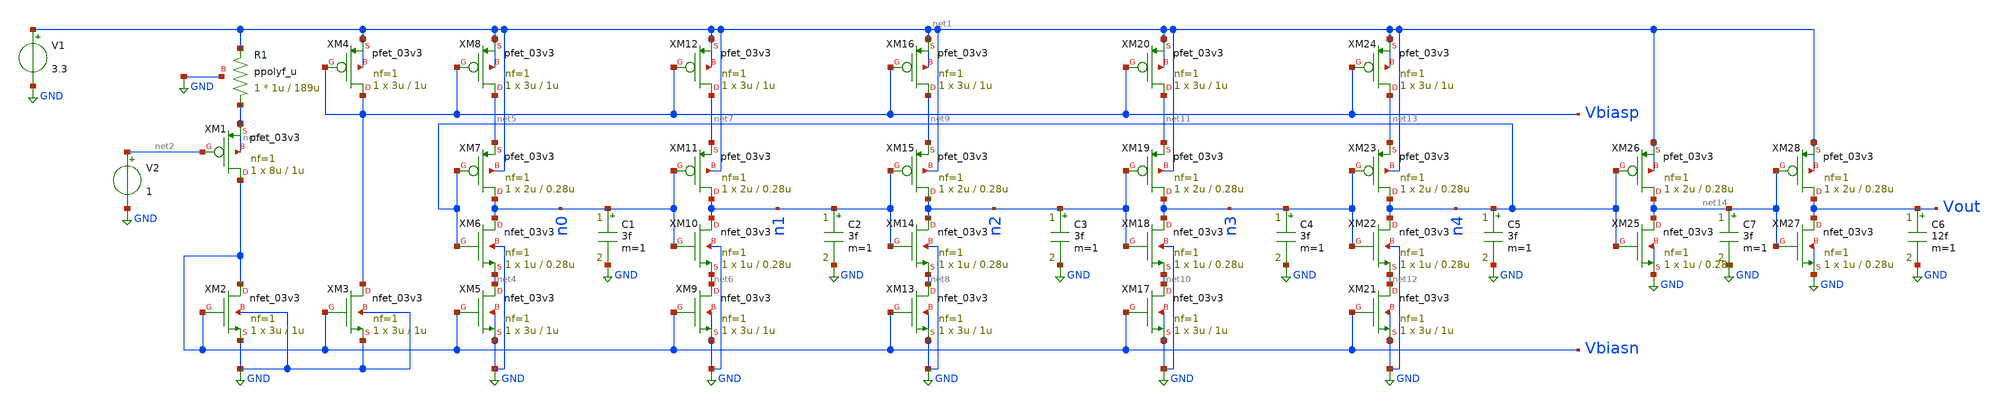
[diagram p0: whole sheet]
** sch_path: analog/vco/vco.sch
**.subckt vco
XM1 Vbiasn net2 net3 net3 pfet_03v3 L=1u W=8u nf=1 ad='int((nf+1)/2) * W/nf * 0.18u' as='int((nf+2)/2) * W/nf * 0.18u'
+ pd='2*int((nf+1)/2) * (W/nf + 0.18u)' ps='2*int((nf+2)/2) * (W/nf + 0.18u)' nrd='0.18u / W' nrs='0.18u / W'
+ sa=0 sb=0 sd=0 m=1
XM2 Vbiasn Vbiasn GND GND nfet_03v3 L=1u W=3u nf=1 ad='int((nf+1)/2) * W/nf * 0.18u' as='int((nf+2)/2) * W/nf * 0.18u'
+ pd='2*int((nf+1)/2) * (W/nf + 0.18u)' ps='2*int((nf+2)/2) * (W/nf + 0.18u)' nrd='0.18u / W' nrs='0.18u / W'
+ sa=0 sb=0 sd=0 m=1
XM3 Vbiasp Vbiasn GND GND nfet_03v3 L=1u W=3u nf=1 ad='int((nf+1)/2) * W/nf * 0.18u' as='int((nf+2)/2) * W/nf * 0.18u'
+ pd='2*int((nf+1)/2) * (W/nf + 0.18u)' ps='2*int((nf+2)/2) * (W/nf + 0.18u)' nrd='0.18u / W' nrs='0.18u / W'
+ sa=0 sb=0 sd=0 m=1
V1 net1 GND 3.3
XM4 Vbiasp Vbiasp net1 net1 pfet_03v3 L=1u W=3u nf=1 ad='int((nf+1)/2) * W/nf * 0.18u' as='int((nf+2)/2) * W/nf * 0.18u'
+ pd='2*int((nf+1)/2) * (W/nf + 0.18u)' ps='2*int((nf+2)/2) * (W/nf + 0.18u)' nrd='0.18u / W' nrs='0.18u / W'
+ sa=0 sb=0 sd=0 m=1
V2 net2 GND 1
XR1 net3 net1 GND ppolyf_u r_width=1u r_length=189u m=1
XM5 net4 Vbiasn GND GND nfet_03v3 L=1u W=3u nf=1 ad='int((nf+1)/2) * W/nf * 0.18u' as='int((nf+2)/2) * W/nf * 0.18u'
+ pd='2*int((nf+1)/2) * (W/nf + 0.18u)' ps='2*int((nf+2)/2) * (W/nf + 0.18u)' nrd='0.18u / W' nrs='0.18u / W'
+ sa=0 sb=0 sd=0 m=1
XM6 n0 n4 net4 GND nfet_03v3 L=0.28u W=1u nf=1 ad='int((nf+1)/2) * W/nf * 0.18u' as='int((nf+2)/2) * W/nf * 0.18u'
+ pd='2*int((nf+1)/2) * (W/nf + 0.18u)' ps='2*int((nf+2)/2) * (W/nf + 0.18u)' nrd='0.18u / W' nrs='0.18u / W'
+ sa=0 sb=0 sd=0 m=1
XM7 n0 n4 net5 net1 pfet_03v3 L=0.28u W=2u nf=1 ad='int((nf+1)/2) * W/nf * 0.18u' as='int((nf+2)/2) * W/nf * 0.18u'
+ pd='2*int((nf+1)/2) * (W/nf + 0.18u)' ps='2*int((nf+2)/2) * (W/nf + 0.18u)' nrd='0.18u / W' nrs='0.18u / W'
+ sa=0 sb=0 sd=0 m=1
XM8 net5 Vbiasp net1 net1 pfet_03v3 L=1u W=3u nf=1 ad='int((nf+1)/2) * W/nf * 0.18u' as='int((nf+2)/2) * W/nf * 0.18u'
+ pd='2*int((nf+1)/2) * (W/nf + 0.18u)' ps='2*int((nf+2)/2) * (W/nf + 0.18u)' nrd='0.18u / W' nrs='0.18u / W'
+ sa=0 sb=0 sd=0 m=1
XM9 net6 Vbiasn GND GND nfet_03v3 L=1u W=3u nf=1 ad='int((nf+1)/2) * W/nf * 0.18u' as='int((nf+2)/2) * W/nf * 0.18u'
+ pd='2*int((nf+1)/2) * (W/nf + 0.18u)' ps='2*int((nf+2)/2) * (W/nf + 0.18u)' nrd='0.18u / W' nrs='0.18u / W'
+ sa=0 sb=0 sd=0 m=1
XM10 n1 n0 net6 GND nfet_03v3 L=0.28u W=1u nf=1 ad='int((nf+1)/2) * W/nf * 0.18u' as='int((nf+2)/2) * W/nf * 0.18u'
+ pd='2*int((nf+1)/2) * (W/nf + 0.18u)' ps='2*int((nf+2)/2) * (W/nf + 0.18u)' nrd='0.18u / W' nrs='0.18u / W'
+ sa=0 sb=0 sd=0 m=1
XM11 n1 n0 net7 net1 pfet_03v3 L=0.28u W=2u nf=1 ad='int((nf+1)/2) * W/nf * 0.18u' as='int((nf+2)/2) * W/nf * 0.18u'
+ pd='2*int((nf+1)/2) * (W/nf + 0.18u)' ps='2*int((nf+2)/2) * (W/nf + 0.18u)' nrd='0.18u / W' nrs='0.18u / W'
+ sa=0 sb=0 sd=0 m=1
XM12 net7 Vbiasp net1 net1 pfet_03v3 L=1u W=3u nf=1 ad='int((nf+1)/2) * W/nf * 0.18u' as='int((nf+2)/2) * W/nf * 0.18u'
+ pd='2*int((nf+1)/2) * (W/nf + 0.18u)' ps='2*int((nf+2)/2) * (W/nf + 0.18u)' nrd='0.18u / W' nrs='0.18u / W'
+ sa=0 sb=0 sd=0 m=1
XM13 net8 Vbiasn GND GND nfet_03v3 L=1u W=3u nf=1 ad='int((nf+1)/2) * W/nf * 0.18u' as='int((nf+2)/2) * W/nf * 0.18u'
+ pd='2*int((nf+1)/2) * (W/nf + 0.18u)' ps='2*int((nf+2)/2) * (W/nf + 0.18u)' nrd='0.18u / W' nrs='0.18u / W'
+ sa=0 sb=0 sd=0 m=1
XM14 n2 n1 net8 GND nfet_03v3 L=0.28u W=1u nf=1 ad='int((nf+1)/2) * W/nf * 0.18u' as='int((nf+2)/2) * W/nf * 0.18u'
+ pd='2*int((nf+1)/2) * (W/nf + 0.18u)' ps='2*int((nf+2)/2) * (W/nf + 0.18u)' nrd='0.18u / W' nrs='0.18u / W'
+ sa=0 sb=0 sd=0 m=1
XM15 n2 n1 net9 net1 pfet_03v3 L=0.28u W=2u nf=1 ad='int((nf+1)/2) * W/nf * 0.18u' as='int((nf+2)/2) * W/nf * 0.18u'
+ pd='2*int((nf+1)/2) * (W/nf + 0.18u)' ps='2*int((nf+2)/2) * (W/nf + 0.18u)' nrd='0.18u / W' nrs='0.18u / W'
+ sa=0 sb=0 sd=0 m=1
XM16 net9 Vbiasp net1 net1 pfet_03v3 L=1u W=3u nf=1 ad='int((nf+1)/2) * W/nf * 0.18u' as='int((nf+2)/2) * W/nf * 0.18u'
+ pd='2*int((nf+1)/2) * (W/nf + 0.18u)' ps='2*int((nf+2)/2) * (W/nf + 0.18u)' nrd='0.18u / W' nrs='0.18u / W'
+ sa=0 sb=0 sd=0 m=1
XM17 net10 Vbiasn GND GND nfet_03v3 L=1u W=3u nf=1 ad='int((nf+1)/2) * W/nf * 0.18u' as='int((nf+2)/2) * W/nf * 0.18u'
+ pd='2*int((nf+1)/2) * (W/nf + 0.18u)' ps='2*int((nf+2)/2) * (W/nf + 0.18u)' nrd='0.18u / W' nrs='0.18u / W'
+ sa=0 sb=0 sd=0 m=1
XM18 n3 n2 net10 GND nfet_03v3 L=0.28u W=1u nf=1 ad='int((nf+1)/2) * W/nf * 0.18u' as='int((nf+2)/2) * W/nf * 0.18u'
+ pd='2*int((nf+1)/2) * (W/nf + 0.18u)' ps='2*int((nf+2)/2) * (W/nf + 0.18u)' nrd='0.18u / W' nrs='0.18u / W'
+ sa=0 sb=0 sd=0 m=1
XM19 n3 n2 net11 net1 pfet_03v3 L=0.28u W=2u nf=1 ad='int((nf+1)/2) * W/nf * 0.18u' as='int((nf+2)/2) * W/nf * 0.18u'
+ pd='2*int((nf+1)/2) * (W/nf + 0.18u)' ps='2*int((nf+2)/2) * (W/nf + 0.18u)' nrd='0.18u / W' nrs='0.18u / W'
+ sa=0 sb=0 sd=0 m=1
XM20 net11 Vbiasp net1 net1 pfet_03v3 L=1u W=3u nf=1 ad='int((nf+1)/2) * W/nf * 0.18u' as='int((nf+2)/2) * W/nf * 0.18u'
+ pd='2*int((nf+1)/2) * (W/nf + 0.18u)' ps='2*int((nf+2)/2) * (W/nf + 0.18u)' nrd='0.18u / W' nrs='0.18u / W'
+ sa=0 sb=0 sd=0 m=1
XM21 net12 Vbiasn GND GND nfet_03v3 L=1u W=3u nf=1 ad='int((nf+1)/2) * W/nf * 0.18u' as='int((nf+2)/2) * W/nf * 0.18u'
+ pd='2*int((nf+1)/2) * (W/nf + 0.18u)' ps='2*int((nf+2)/2) * (W/nf + 0.18u)' nrd='0.18u / W' nrs='0.18u / W'
+ sa=0 sb=0 sd=0 m=1
XM22 n4 n3 net12 GND nfet_03v3 L=0.28u W=1u nf=1 ad='int((nf+1)/2) * W/nf * 0.18u' as='int((nf+2)/2) * W/nf * 0.18u'
+ pd='2*int((nf+1)/2) * (W/nf + 0.18u)' ps='2*int((nf+2)/2) * (W/nf + 0.18u)' nrd='0.18u / W' nrs='0.18u / W'
+ sa=0 sb=0 sd=0 m=1
XM23 n4 n3 net13 net1 pfet_03v3 L=0.28u W=2u nf=1 ad='int((nf+1)/2) * W/nf * 0.18u' as='int((nf+2)/2) * W/nf * 0.18u'
+ pd='2*int((nf+1)/2) * (W/nf + 0.18u)' ps='2*int((nf+2)/2) * (W/nf + 0.18u)' nrd='0.18u / W' nrs='0.18u / W'
+ sa=0 sb=0 sd=0 m=1
XM24 net13 Vbiasp net1 net1 pfet_03v3 L=1u W=3u nf=1 ad='int((nf+1)/2) * W/nf * 0.18u' as='int((nf+2)/2) * W/nf * 0.18u'
+ pd='2*int((nf+1)/2) * (W/nf + 0.18u)' ps='2*int((nf+2)/2) * (W/nf + 0.18u)' nrd='0.18u / W' nrs='0.18u / W'
+ sa=0 sb=0 sd=0 m=1
C1 n0 GND 3f m=1
C2 n1 GND 3f m=1
C3 n2 GND 3f m=1
C4 n3 GND 3f m=1
C5 n4 GND 3f m=1
XM25 net14 n4 GND GND nfet_03v3 L=0.28u W=1u nf=1 ad='int((nf+1)/2) * W/nf * 0.18u' as='int((nf+2)/2) * W/nf * 0.18u'
+ pd='2*int((nf+1)/2) * (W/nf + 0.18u)' ps='2*int((nf+2)/2) * (W/nf + 0.18u)' nrd='0.18u / W' nrs='0.18u / W'
+ sa=0 sb=0 sd=0 m=1
XM26 net14 n4 net1 net1 pfet_03v3 L=0.28u W=2u nf=1 ad='int((nf+1)/2) * W/nf * 0.18u' as='int((nf+2)/2) * W/nf * 0.18u'
+ pd='2*int((nf+1)/2) * (W/nf + 0.18u)' ps='2*int((nf+2)/2) * (W/nf + 0.18u)' nrd='0.18u / W' nrs='0.18u / W'
+ sa=0 sb=0 sd=0 m=1
XM27 Vout net14 GND GND nfet_03v3 L=0.28u W=1u nf=1 ad='int((nf+1)/2) * W/nf * 0.18u' as='int((nf+2)/2) * W/nf * 0.18u'
+ pd='2*int((nf+1)/2) * (W/nf + 0.18u)' ps='2*int((nf+2)/2) * (W/nf + 0.18u)' nrd='0.18u / W' nrs='0.18u / W'
+ sa=0 sb=0 sd=0 m=1
XM28 Vout net14 net1 net1 pfet_03v3 L=0.28u W=2u nf=1 ad='int((nf+1)/2) * W/nf * 0.18u' as='int((nf+2)/2) * W/nf * 0.18u'
+ pd='2*int((nf+1)/2) * (W/nf + 0.18u)' ps='2*int((nf+2)/2) * (W/nf + 0.18u)' nrd='0.18u / W' nrs='0.18u / W'
+ sa=0 sb=0 sd=0 m=1
C6 Vout GND 12f m=1
C7 net14 GND 3f m=1
**** begin user architecture code

.include /usr/local/share/pdk/gf180mcuD/libs.tech/ngspice/design.ngspice
.lib /usr/local/share/pdk/gf180mcuD/libs.tech/ngspice/sm141064.ngspice typical
.lib /usr/local/share/pdk/gf180mcuD/libs.tech/ngspice/sm141064.ngspice res_typical
.ic v(n0)=0 v(n1)=3.3 v(n2)=0 v(n3)=3.3 v(n4)=0
.control
dc V2 0 3.3 0.01
plot v(vbiasn) v(vbiasp) xlabel Vctrl ylabel Volts title Bias_voltages
setplot new
set results = $curplot
let vc = vector(21)*0.1
let f = vector(21)*0
let i = 0
while i < 21
  let vnow = vc[i]
  alter V2 dc = $&vnow
  tran 100p 1.6u 0 100p
  set runplot = $curplot
  meas tran t1 when v(n0)=1.65 rise=8
  meas tran t2 when v(n0)=1.65 rise=28
  let fnow = 20/(t2-t1)/1e6
  set fval = $&fnow
  setplot $results
  let f[i] = $fval
  destroy $runplot
  let i = i + 1
end
print vc f
plot f vs vc xlabel Vctrl ylabel MHz title VCO_frequency
alter V2 dc = 1
alter C6 = 5f
tran 20p 540n 0 20p
let n4in = v(n4)
let v5f = v(vout)
set p5 = $curplot
alter C6 = 10f
tran 20p 540n 0 20p
let v10f = v(vout)
set p10 = $curplot
alter C6 = 15f
tran 20p 540n 0 20p
let v15f = v(vout)
set p15 = $curplot
plot {$p5}.n4in {$p5}.v5f {$p10}.v10f {$p15}.v15f xlimit 500n 540n title C6_sweep
plot v(n0) v(n1) v(n2) xlimit 500n 540n xlabel Time ylabel Volts title Ring_nodes
alter C6 = 20f
.endc


**** end user architecture code
**.ends
.GLOBAL GND
.end
